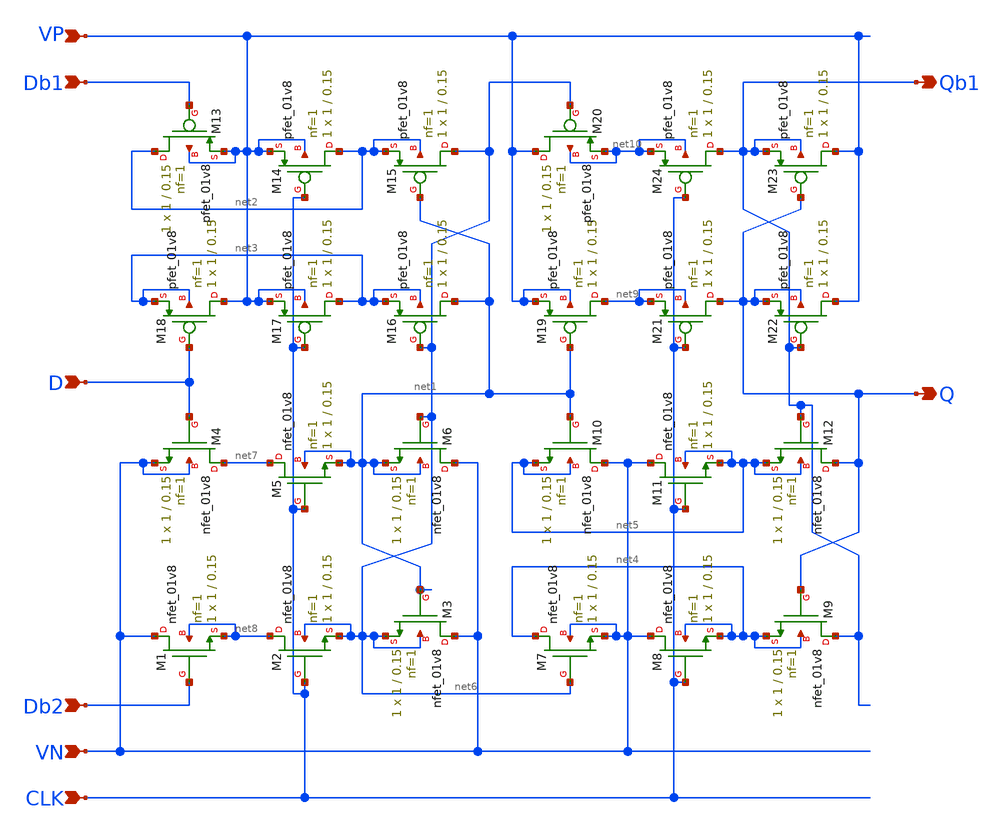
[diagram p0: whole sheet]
** sch_path: projects/negdff/xschem_ngspice/negdff2.sch
**.subckt negdff2 D Db1 Db2 Q Qb1 CLK VP VN
*.ipin D
*.ipin Db1
*.ipin Db2
*.opin Q
*.opin Qb1
*.ipin CLK
*.ipin VP
*.ipin VN
XM1 VN Db2 net8 net8 sky130_fd_pr__nfet_01v8 L=0.15 W=1 nf=1 ad='int((nf+1)/2) * W/nf * 0.29' as='int((nf+2)/2) * W/nf * 0.29'
+ pd='2*int((nf+1)/2) * (W/nf + 0.29)' ps='2*int((nf+2)/2) * (W/nf + 0.29)' nrd='0.29 / W' nrs='0.29 / W'
+ sa=0 sb=0 sd=0 mult=1 m=1
XM2 net8 CLK net6 net6 sky130_fd_pr__nfet_01v8 L=0.15 W=1 nf=1 ad='int((nf+1)/2) * W/nf * 0.29' as='int((nf+2)/2) * W/nf * 0.29'
+ pd='2*int((nf+1)/2) * (W/nf + 0.29)' ps='2*int((nf+2)/2) * (W/nf + 0.29)' nrd='0.29 / W' nrs='0.29 / W'
+ sa=0 sb=0 sd=0 mult=1 m=1
XM3 VN net1 net6 net6 sky130_fd_pr__nfet_01v8 L=0.15 W=1 nf=1 ad='int((nf+1)/2) * W/nf * 0.29' as='int((nf+2)/2) * W/nf * 0.29'
+ pd='2*int((nf+1)/2) * (W/nf + 0.29)' ps='2*int((nf+2)/2) * (W/nf + 0.29)' nrd='0.29 / W' nrs='0.29 / W'
+ sa=0 sb=0 sd=0 mult=1 m=1
XM4 net7 D VN VN sky130_fd_pr__nfet_01v8 L=0.15 W=1 nf=1 ad='int((nf+1)/2) * W/nf * 0.29' as='int((nf+2)/2) * W/nf * 0.29'
+ pd='2*int((nf+1)/2) * (W/nf + 0.29)' ps='2*int((nf+2)/2) * (W/nf + 0.29)' nrd='0.29 / W' nrs='0.29 / W'
+ sa=0 sb=0 sd=0 mult=1 m=1
XM5 net7 CLK net1 net1 sky130_fd_pr__nfet_01v8 L=0.15 W=1 nf=1 ad='int((nf+1)/2) * W/nf * 0.29' as='int((nf+2)/2) * W/nf * 0.29'
+ pd='2*int((nf+1)/2) * (W/nf + 0.29)' ps='2*int((nf+2)/2) * (W/nf + 0.29)' nrd='0.29 / W' nrs='0.29 / W'
+ sa=0 sb=0 sd=0 mult=1 m=1
XM6 VN net6 net1 net1 sky130_fd_pr__nfet_01v8 L=0.15 W=1 nf=1 ad='int((nf+1)/2) * W/nf * 0.29' as='int((nf+2)/2) * W/nf * 0.29'
+ pd='2*int((nf+1)/2) * (W/nf + 0.29)' ps='2*int((nf+2)/2) * (W/nf + 0.29)' nrd='0.29 / W' nrs='0.29 / W'
+ sa=0 sb=0 sd=0 mult=1 m=1
XM7 net4 net6 VN VN sky130_fd_pr__nfet_01v8 L=0.15 W=1 nf=1 ad='int((nf+1)/2) * W/nf * 0.29' as='int((nf+2)/2) * W/nf * 0.29'
+ pd='2*int((nf+1)/2) * (W/nf + 0.29)' ps='2*int((nf+2)/2) * (W/nf + 0.29)' nrd='0.29 / W' nrs='0.29 / W'
+ sa=0 sb=0 sd=0 mult=1 m=1
XM8 VN CLK net4 net4 sky130_fd_pr__nfet_01v8 L=0.15 W=1 nf=1 ad='int((nf+1)/2) * W/nf * 0.29' as='int((nf+2)/2) * W/nf * 0.29'
+ pd='2*int((nf+1)/2) * (W/nf + 0.29)' ps='2*int((nf+2)/2) * (W/nf + 0.29)' nrd='0.29 / W' nrs='0.29 / W'
+ sa=0 sb=0 sd=0 mult=1 m=1
XM9 Qb1 Q net4 net4 sky130_fd_pr__nfet_01v8 L=0.15 W=1 nf=1 ad='int((nf+1)/2) * W/nf * 0.29' as='int((nf+2)/2) * W/nf * 0.29'
+ pd='2*int((nf+1)/2) * (W/nf + 0.29)' ps='2*int((nf+2)/2) * (W/nf + 0.29)' nrd='0.29 / W' nrs='0.29 / W'
+ sa=0 sb=0 sd=0 mult=1 m=1
XM10 VN net1 net5 net5 sky130_fd_pr__nfet_01v8 L=0.15 W=1 nf=1 ad='int((nf+1)/2) * W/nf * 0.29' as='int((nf+2)/2) * W/nf * 0.29'
+ pd='2*int((nf+1)/2) * (W/nf + 0.29)' ps='2*int((nf+2)/2) * (W/nf + 0.29)' nrd='0.29 / W' nrs='0.29 / W'
+ sa=0 sb=0 sd=0 mult=1 m=1
XM11 VN CLK net5 net5 sky130_fd_pr__nfet_01v8 L=0.15 W=1 nf=1 ad='int((nf+1)/2) * W/nf * 0.29' as='int((nf+2)/2) * W/nf * 0.29'
+ pd='2*int((nf+1)/2) * (W/nf + 0.29)' ps='2*int((nf+2)/2) * (W/nf + 0.29)' nrd='0.29 / W' nrs='0.29 / W'
+ sa=0 sb=0 sd=0 mult=1 m=1
XM12 Q Qb1 net5 net5 sky130_fd_pr__nfet_01v8 L=0.15 W=1 nf=1 ad='int((nf+1)/2) * W/nf * 0.29' as='int((nf+2)/2) * W/nf * 0.29'
+ pd='2*int((nf+1)/2) * (W/nf + 0.29)' ps='2*int((nf+2)/2) * (W/nf + 0.29)' nrd='0.29 / W' nrs='0.29 / W'
+ sa=0 sb=0 sd=0 mult=1 m=1
XM13 net2 Db1 VP VP sky130_fd_pr__pfet_01v8 L=0.15 W=1 nf=1 ad='int((nf+1)/2) * W/nf * 0.29' as='int((nf+2)/2) * W/nf * 0.29'
+ pd='2*int((nf+1)/2) * (W/nf + 0.29)' ps='2*int((nf+2)/2) * (W/nf + 0.29)' nrd='0.29 / W' nrs='0.29 / W'
+ sa=0 sb=0 sd=0 mult=1 m=1
XM14 net2 CLK VP VP sky130_fd_pr__pfet_01v8 L=0.15 W=1 nf=1 ad='int((nf+1)/2) * W/nf * 0.29' as='int((nf+2)/2) * W/nf * 0.29'
+ pd='2*int((nf+1)/2) * (W/nf + 0.29)' ps='2*int((nf+2)/2) * (W/nf + 0.29)' nrd='0.29 / W' nrs='0.29 / W'
+ sa=0 sb=0 sd=0 mult=1 m=1
XM15 net6 net1 net2 net2 sky130_fd_pr__pfet_01v8 L=0.15 W=1 nf=1 ad='int((nf+1)/2) * W/nf * 0.29' as='int((nf+2)/2) * W/nf * 0.29'
+ pd='2*int((nf+1)/2) * (W/nf + 0.29)' ps='2*int((nf+2)/2) * (W/nf + 0.29)' nrd='0.29 / W' nrs='0.29 / W'
+ sa=0 sb=0 sd=0 mult=1 m=1
XM16 net1 net6 net3 net3 sky130_fd_pr__pfet_01v8 L=0.15 W=1 nf=1 ad='int((nf+1)/2) * W/nf * 0.29' as='int((nf+2)/2) * W/nf * 0.29'
+ pd='2*int((nf+1)/2) * (W/nf + 0.29)' ps='2*int((nf+2)/2) * (W/nf + 0.29)' nrd='0.29 / W' nrs='0.29 / W'
+ sa=0 sb=0 sd=0 mult=1 m=1
XM17 net3 CLK VP VP sky130_fd_pr__pfet_01v8 L=0.15 W=1 nf=1 ad='int((nf+1)/2) * W/nf * 0.29' as='int((nf+2)/2) * W/nf * 0.29'
+ pd='2*int((nf+1)/2) * (W/nf + 0.29)' ps='2*int((nf+2)/2) * (W/nf + 0.29)' nrd='0.29 / W' nrs='0.29 / W'
+ sa=0 sb=0 sd=0 mult=1 m=1
XM18 VP D net3 net3 sky130_fd_pr__pfet_01v8 L=0.15 W=1 nf=1 ad='int((nf+1)/2) * W/nf * 0.29' as='int((nf+2)/2) * W/nf * 0.29'
+ pd='2*int((nf+1)/2) * (W/nf + 0.29)' ps='2*int((nf+2)/2) * (W/nf + 0.29)' nrd='0.29 / W' nrs='0.29 / W'
+ sa=0 sb=0 sd=0 mult=1 m=1
XM19 net9 net1 VP VP sky130_fd_pr__pfet_01v8 L=0.15 W=1 nf=1 ad='int((nf+1)/2) * W/nf * 0.29' as='int((nf+2)/2) * W/nf * 0.29'
+ pd='2*int((nf+1)/2) * (W/nf + 0.29)' ps='2*int((nf+2)/2) * (W/nf + 0.29)' nrd='0.29 / W' nrs='0.29 / W'
+ sa=0 sb=0 sd=0 mult=1 m=1
XM20 VP net6 net10 net10 sky130_fd_pr__pfet_01v8 L=0.15 W=1 nf=1 ad='int((nf+1)/2) * W/nf * 0.29' as='int((nf+2)/2) * W/nf * 0.29'
+ pd='2*int((nf+1)/2) * (W/nf + 0.29)' ps='2*int((nf+2)/2) * (W/nf + 0.29)' nrd='0.29 / W' nrs='0.29 / W'
+ sa=0 sb=0 sd=0 mult=1 m=1
XM21 Q CLK net9 net9 sky130_fd_pr__pfet_01v8 L=0.15 W=1 nf=1 ad='int((nf+1)/2) * W/nf * 0.29' as='int((nf+2)/2) * W/nf * 0.29'
+ pd='2*int((nf+1)/2) * (W/nf + 0.29)' ps='2*int((nf+2)/2) * (W/nf + 0.29)' nrd='0.29 / W' nrs='0.29 / W'
+ sa=0 sb=0 sd=0 mult=1 m=1
XM22 VP Qb1 Q Q sky130_fd_pr__pfet_01v8 L=0.15 W=1 nf=1 ad='int((nf+1)/2) * W/nf * 0.29' as='int((nf+2)/2) * W/nf * 0.29'
+ pd='2*int((nf+1)/2) * (W/nf + 0.29)' ps='2*int((nf+2)/2) * (W/nf + 0.29)' nrd='0.29 / W' nrs='0.29 / W'
+ sa=0 sb=0 sd=0 mult=1 m=1
XM23 VP Q Qb1 Qb1 sky130_fd_pr__pfet_01v8 L=0.15 W=1 nf=1 ad='int((nf+1)/2) * W/nf * 0.29' as='int((nf+2)/2) * W/nf * 0.29'
+ pd='2*int((nf+1)/2) * (W/nf + 0.29)' ps='2*int((nf+2)/2) * (W/nf + 0.29)' nrd='0.29 / W' nrs='0.29 / W'
+ sa=0 sb=0 sd=0 mult=1 m=1
XM24 Qb1 CLK net10 net10 sky130_fd_pr__pfet_01v8 L=0.15 W=1 nf=1 ad='int((nf+1)/2) * W/nf * 0.29' as='int((nf+2)/2) * W/nf * 0.29'
+ pd='2*int((nf+1)/2) * (W/nf + 0.29)' ps='2*int((nf+2)/2) * (W/nf + 0.29)' nrd='0.29 / W' nrs='0.29 / W'
+ sa=0 sb=0 sd=0 mult=1 m=1
**.ends
.end
